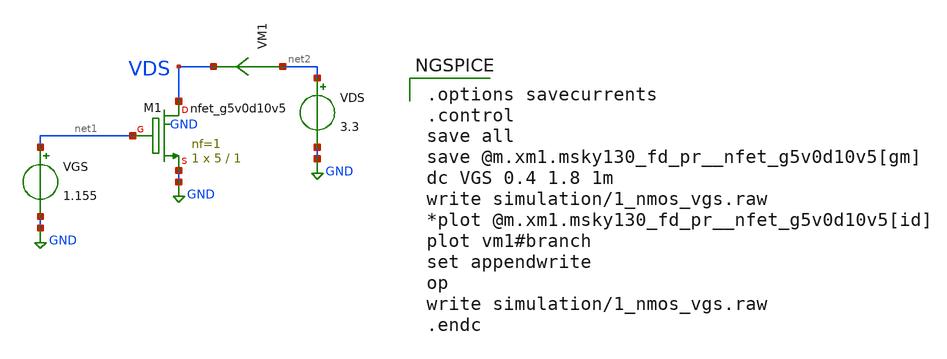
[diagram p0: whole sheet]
** sch_path: xschem/1_nmos_vgs.sch
**.subckt 1_nmos_vgs
XM1 VDS net1 GND GND sky130_fd_pr__nfet_g5v0d10v5 L=1 W=5 nf=1 ad='int((nf+1)/2) * W/nf * 0.29' as='int((nf+2)/2) * W/nf * 0.29'
+ pd='2*int((nf+1)/2) * (W/nf + 0.29)' ps='2*int((nf+2)/2) * (W/nf + 0.29)' nrd='0.29 / W' nrs='0.29 / W'
+ sa=0 sb=0 sd=0 mult=1 m=1
VGS net1 GND 1.155
VDS net2 GND 3.3
VM1 net2 VDS 0
.save i(vm1)
**** begin user architecture code

.options savecurrents
.control
save all
save @m.xm1.msky130_fd_pr__nfet_g5v0d10v5[gm]
dc VGS 0.4 1.8 1m
write simulation/1_nmos_vgs.raw
*plot @m.xm1.msky130_fd_pr__nfet_g5v0d10v5[id]
plot vm1#branch
set appendwrite
op
write simulation/1_nmos_vgs.raw
.endc



** opencircuitdesign pdks install
.lib $::SKYWATER_MODELS/sky130.lib.spice tt


**** end user architecture code
**.ends
.GLOBAL GND
.end
